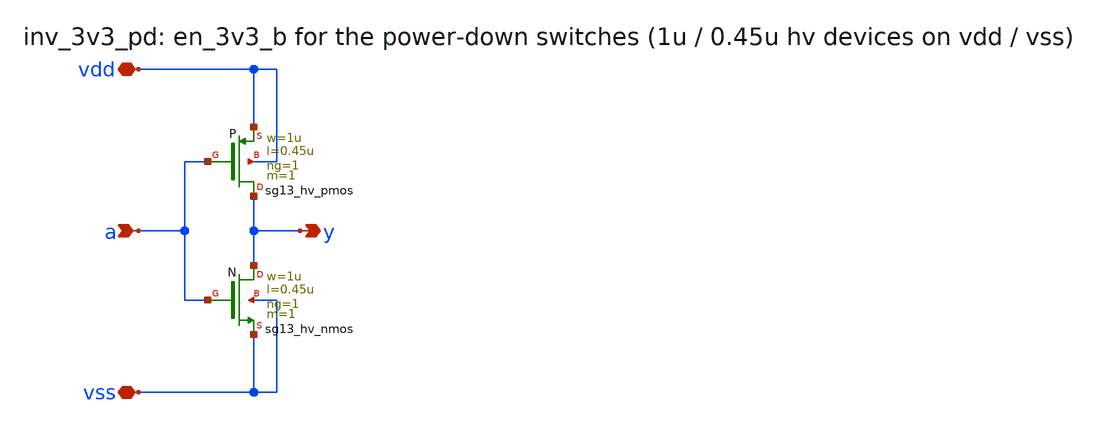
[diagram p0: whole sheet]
** sch_path: macros/d2s_bias_sel_pd/schematic/xschem/inv_3v3_pd.sch
**.subckt inv_3v3_pd vdd vss a y
*.iopin vdd
*.iopin vss
*.ipin a
*.opin y
XP y a vdd vdd sg13_hv_pmos w=1u l=0.45u ng=1 m=1 mm_ok=1
XN y a vss vss sg13_hv_nmos w=1u l=0.45u ng=1 m=1 mm_ok=1
**.ends
.end
